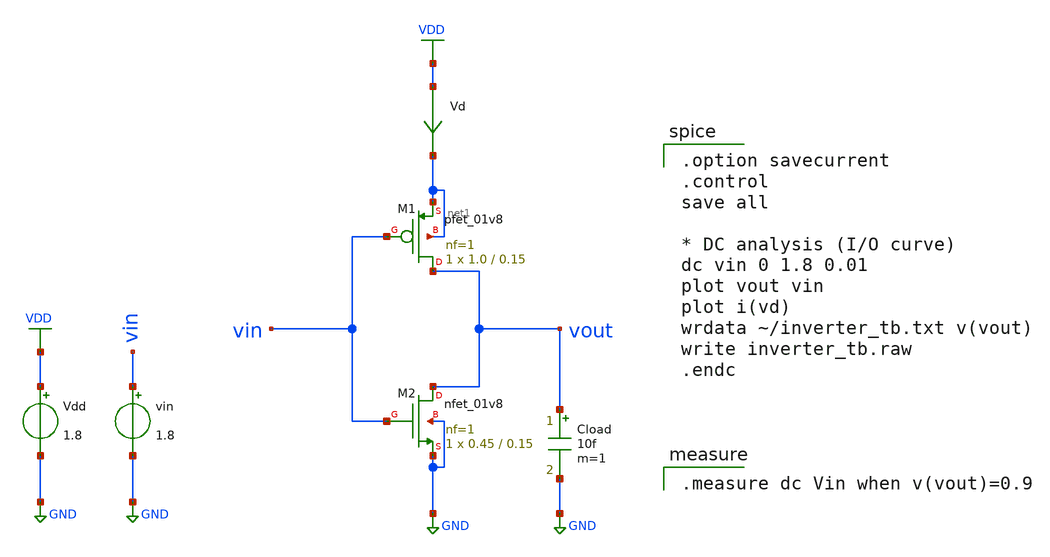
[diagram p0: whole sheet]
** sch_path: samples/inverter/SKY130/inverter_tb.sch
**.subckt inverter_tb
Vdd VDD GND 1.8
vin vin GND 1.8
Vd VDD net1 0
.save i(vd)
Cload vout GND 10f m=1
XM1 vout vin net1 net1 sky130_fd_pr__pfet_01v8 L=0.15 W=1.0 nf=1 ad='int((1 + 1)/2) * 1.0 / 1 * 0.29'
+ as='int((1 + 2)/2) * 1.0 / 1 * 0.29' pd='2*int((1 + 1)/2) * (1.0 / 1 + 0.29)' ps='2*int((1 + 2)/2) * (1.0 / 1 + 0.29)'
+ nrd='0.29 / 1.0 ' nrs='0.29 / 1.0 ' sa=0 sb=0 sd=0 mult=1 m=1
XM2 vout vin GND GND sky130_fd_pr__nfet_01v8 L=0.15 W=0.45 nf=1 ad='int((1 + 1)/2) * 0.45 / 1 * 0.29'
+ as='int((1 + 2)/2) * 0.45 / 1 * 0.29' pd='2*int((1 + 1)/2) * (0.45 / 1 + 0.29)' ps='2*int((1 + 2)/2) * (0.45 / 1 + 0.29)'
+ nrd='0.29 / 0.45 ' nrs='0.29 / 0.45 ' sa=0 sb=0 sd=0 mult=1 m=1
**** begin user architecture code

.option savecurrent
.control
save all

* DC analysis (I/O curve)
dc vin 0 1.8 0.01
plot vout vin
plot i(vd)
wrdata ~/inverter_tb.txt v(vout)
write inverter_tb.raw
.endc


.measure dc Vin when v(vout)=0.9


** opencircuitdesign pdks install
.lib $::SKYWATER_MODELS/sky130.lib.spice tt

**** end user architecture code
**.ends
.GLOBAL GND
.GLOBAL VDD
.end
